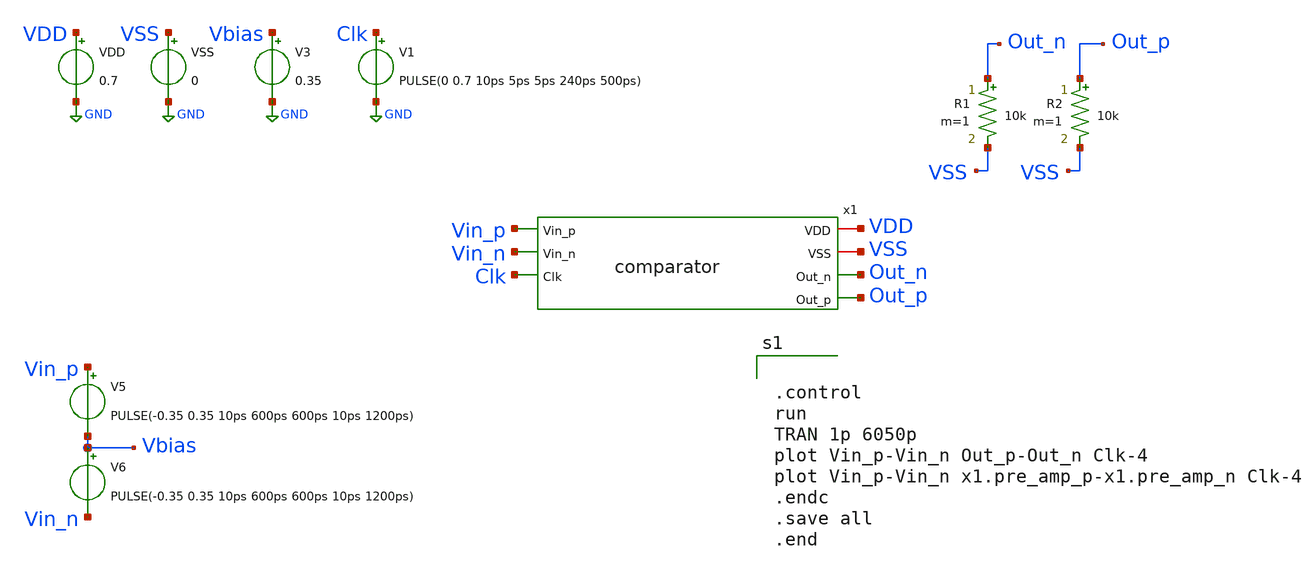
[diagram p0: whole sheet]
** sch_path: xschem/test/comparator_test_triangular_input.sch
* xschem/lib/asap_7nm_nfet.sym:
* Copyright 2021 Stefan Frederik Schippers
* Licensed under the Apache License, Version 2.0 (the "License");
**.subckt comparator_test_triangular_input
V5 Vin_p Vbias PULSE(-0.35 0.35 10ps 600ps 600ps 10ps 1200ps)
V6 Vbias Vin_n PULSE(-0.35 0.35 10ps 600ps 600ps 10ps 1200ps)
VDD VDD GND 0.7
VSS VSS GND 0
V1 Clk GND PULSE(0 0.7 10ps 5ps 5ps 240ps 500ps)
V3 Vbias GND 0.35
R1 Out_n VSS 10k m=1
R2 Out_p VSS 10k m=1
x1 VDD VSS Vin_p Out_n Vin_n Clk Out_p comparator
**** begin user architecture code


.control
run
TRAN 1p 6050p
plot Vin_p-Vin_n Out_p-Out_n Clk-4
plot Vin_p-Vin_n x1.pre_amp_p-x1.pre_amp_n Clk-4
.endc
.save all
.end


**** end user architecture code
**.ends

* expanding   symbol:  /media/psf/avsdcmp_7nm/xschem/src/comparator.sym # of pins=7
** sym_path: xschem/src/comparator.sym
** sch_path: xschem/src/comparator.sch
.subckt comparator VDD VSS Vin_p Out_n Vin_n Clk Out_p
*.iopin VDD
*.iopin VSS
*.ipin Vin_p
*.opin Out_n
*.ipin Vin_n
*.opin Out_p
*.ipin Clk
Xpfet1 Pre_Amp_n Clk_buf VDD VDD asap_7nm_pfet l=7e-009 nfin=7
Xpfet2 Pre_Amp_p Clk_buf VDD VDD asap_7nm_pfet l=7e-009 nfin=7
Xnfet1 Pre_Amp_n Vin_p net1 VSS asap_7nm_nfet l=7e-009 nfin=14
Xnfet2 Pre_Amp_p Vin_n net1 VSS asap_7nm_nfet l=7e-009 nfin=14
Xnfet3 net1 Clk_buf VSS VSS asap_7nm_nfet l=7e-009 nfin=14
Xpfet3 net2 net4 VDD VDD asap_7nm_pfet l=7e-009 nfin=2
Xpfet4 net3 net5 VDD VDD asap_7nm_pfet l=7e-009 nfin=2
Xpfet5 net5 Pre_Amp_n net2 VDD asap_7nm_pfet l=7e-009 nfin=4
Xpfet6 net4 Pre_Amp_p net3 VDD asap_7nm_pfet l=7e-009 nfin=4
Xnfet4 net5 Clk_n VSS VSS asap_7nm_nfet l=7e-009 nfin=10
Xnfet5 net5 net4 VSS VSS asap_7nm_nfet l=7e-009 nfin=10
Xnfet6 net4 net5 VSS VSS asap_7nm_nfet l=7e-009 nfin=10
Xnfet7 net4 Clk_n VSS VSS asap_7nm_nfet l=7e-009 nfin=10
Xpfet7 Clk_n Clk VDD VDD asap_7nm_pfet l=7e-009 nfin=14
Xnfet8 Clk_n Clk VSS VSS asap_7nm_nfet l=7e-009 nfin=14
x3 Out_p net6 VDD VSS buf8
x1 net6 net5 VSS VDD buf8
x2 Out_n net7 VDD VSS buf8
x10 net7 net4 VSS VDD buf8
x4 Clk_buf Clk VDD VSS buf8
.ends


* expanding   symbol:  buf8.sym # of pins=4
** sym_path: xschem/lib/buf8.sym
** sch_path: xschem/lib/buf8.sch
.subckt buf8 Out In VDD VSS
*.iopin VDD
*.iopin VSS
*.ipin In
*.opin Out
Xpfet1 net1 In VDD VDD asap_7nm_pfet l=7e-009 nfin=8
Xnfet1 net1 In VSS VSS asap_7nm_nfet l=7e-009 nfin=8
Xpfet2 Out net1 VDD VDD asap_7nm_pfet l=7e-009 nfin=8
Xnfet2 Out net1 VSS VSS asap_7nm_nfet l=7e-009 nfin=8
.ends

.GLOBAL GND
**** begin user architecture code

.subckt asap_7nm_nfet S G D B l=@l nfin=@nfin
	nnmos_finfet S G D B BSIMCMG_osdi_N l=@l nfin=@nfin
.ends asap_7nm_nfet

.model BSIMCMG_osdi_N BSIMCMG_va (  TYPE = 1
************************************************************
*                         general                          *
************************************************************ version = 107             bulkmod = 1
*+               igcmod  = 1               igbmod  = 0              gidlmod = 1               iimod   = 0
*+               geomod  = 1               rdsmod  = 0              rgatemod= 0               rgeomod = 0
*+               shmod   = 0               nqsmod  = 0              coremod = 0               cgeomod = 0
*+               capmod  = 0               tnom    = 25             eot     = 1e-009          eotbox  = 1.4e-007
*+        eotacc  = 1e-010          tfin    = 6.5e-009       toxp    = 2.1e-009        nbody   = 1e+022
*+          phig    = 4.2466          epsrox  = 3.9            epsrsub = 11.9            easub   = 4.05
*+            ni0sub  = 1.1e+016        bg0sub  = 1.17           nc0sub  = 2.86e+025       nsd     = 2e+026
*+          ngate   = 0               nseg    = 5              l       = 2.1e-008        xl      = 1e-009
*+          lint    = -2e-009         dlc     = 0              dlbin   = 0               hfin    = 3.2e-008
*+        deltaw  = 0               deltawcv= 0              sdterm  = 0               epsrsp  = 3.9
*+             nfin    = 1 toxg    = 1.80e-009
************************************************************
*                            dc                            *
************************************************************ cit     = 0               cdsc    =
*+ 0.01            cdscd   = 0.01            dvt0    = 0.05           dvt1    = 0.47            phin    =
*+ 0.05            eta0    = 0.07            dsub    = 0.35           k1rsce  = 0               lpe0    = 0
*+               dvtshift= 0               qmfactor= 2.5            etaqm   = 0.54            qm0     = 0.001           pqm
*+     = 0.66            u0      = 0.0303         etamob  = 2               up      = 0               ua
*+      = 0.55            eu      = 1.2            ud      = 0               ucs     = 1
*+               rdswmin = 0               rdsw    = 200            wr      = 1               rswmin  = 0
*+               rdwmin  = 0               rshs    = 0              rshd    = 0               vsat    = 70000
*+           deltavsat= 0.2             ksativ  = 2              mexp    = 4               ptwg    = 30              pclm
*+    = 0.05            pclmg   = 0              pdibl1  = 0               pdibl2  = 0.002           drout
*+   = 1               pvag    = 0              fpitch  = 2.7e-008        rth0    = 0.225           cth0
*+    = 1.243e-006      wth0    = 2.6e-007       lcdscd  = 5e-005          lcdscdr = 5e-005          lrdsw
*+   = 0.2             lvsat   = 0
************************************************************
*                         leakage                          *
************************************************************ aigc    = 0.014           bigc    =
*+ 0.005           cigc    = 0.25            dlcigs  = 1e-009         dlcigd  = 1e-009          aigs    =
*+ 0.0115          aigd    = 0.0115          bigs    = 0.00332        bigd    = 0.00332         cigs    =
*+ 0.35            cigd    = 0.35            poxedge = 1.1            agidl   = 1e-012          agisl   =
*+ 1e-012          bgidl   = 10000000        bgisl   = 10000000       egidl   = 0.35            egisl   =
*+ 0.35
************************************************************
*                            rf                            *
************************************************************
************************************************************
*                         junction                         *
************************************************************
************************************************************
*                       capacitance                        *
************************************************************ cfs     = 0               cfd     = 0
*+               cgso    = 1.6e-010        cgdo    = 1.6e-010       cgsl    = 0               cgdl    = 0
*+               ckappas = 0.6             ckappad = 0.6            cgbo    = 0               cgbl    = 0
************************************************************
*                       temperature                        *
************************************************************ tbgasub = 0.000473        tbgbsub = 636
*+             kt1     = 0               kt1l    = 0              ute     = -0.7            utl     = 0
*+               ua1     = 0.001032        ud1     = 0              ucste   = -0.004775       at      = 0.001
*+           ptwgt   = 0.004           tmexp   = 0              prt     = 0               tgidl   = -0.007
*+          igt     = 2.5
************************************************************
*                          noise                           *
************************************************************
**)
.control
pre_osdi ~/ASAP7_FinFET_Inverter_Characterization/Xschem_ASAP7/bsimcmg_arch64.osdi
.endc



.subckt asap_7nm_pfet S G D B l=@l nfin=@nfin
	npmos_finfet S G D B BSIMCMG_osdi_P l=@l nfin=@nfin
.ends asap_7nm_pfet

.model BSIMCMG_osdi_P BSIMCMG_va (  TYPE = 0

************************************************************
*                         general                          *
************************************************************ version = 107             bulkmod = 1
*+               igcmod  = 1               igbmod  = 0              gidlmod = 1               iimod   = 0
*+               geomod  = 1               rdsmod  = 0              rgatemod= 0               rgeomod = 0
*+               shmod   = 0               nqsmod  = 0              coremod = 0               cgeomod = 0
*+               capmod  = 0               tnom    = 25             eot     = 1e-009          eotbox  = 1.4e-007
*+        eotacc  = 3e-010          tfin    = 6.5e-009       toxp    = 2.1e-009        nbody   = 1e+022
*+          phig    = 4.9278          epsrox  = 3.9            epsrsub = 11.9            easub   = 4.05
*+            ni0sub  = 1.1e+016        bg0sub  = 1.17           nc0sub  = 2.86e+025       nsd     = 2e+026
*+          ngate   = 0               nseg    = 5              l       = 2.1e-008        xl      = 1e-009
*+          lint    = -2.5e-009       dlc     = 0              dlbin   = 0               hfin    = 3.2e-008
*+        deltaw  = 0               deltawcv= 0              sdterm  = 0               epsrsp  = 3.9
*+             nfin    = 1 toxg    = 1.8e-009
************************************************************
*                            dc                            *
************************************************************ cit     = 0               cdsc    =
*+ 0.003469        cdscd   = 0.001486        dvt0    = 0.05           dvt1    = 0.36            phin    = 0.05
*+            eta0    = 0.094           dsub    = 0.24           k1rsce  = 0               lpe0    = 0
*+               dvtshift= 0               qmfactor= 0              etaqm   = 0.54            qm0     = 2.183e-012      pqm
*+     = 0.66            u0      = 0.0237         etamob  = 4               up      = 0               ua
*+      = 1.133           eu      = 0.05           ud      = 0.0105          ucs     = 0.2672
*+          rdswmin = 0               rdsw    = 200            wr      = 1               rswmin  = 0
*+               rdwmin  = 0               rshs    = 0              rshd    = 0               vsat    = 60000
*+           deltavsat= 0.17            ksativ  = 1.592          mexp    = 2.491           ptwg    = 25              pclm
*+    = 0.01            pclmg   = 1              pdibl1  = 800             pdibl2  = 0.005704        drout
*+   = 4.97            pvag    = 200            fpitch  = 2.7e-008        rth0    = 0.15            cth0
*+    = 1.243e-006      wth0    = 2.6e-007       lcdscd  = 0               lcdscdr = 0               lrdsw
*+   = 1.3             lvsat   = 1441
************************************************************
*                         leakage                          *
************************************************************ aigc    = 0.007           bigc    =
*+ 0.0015          cigc    = 1               dlcigs  = 5e-009         dlcigd  = 5e-009          aigs    =
*+ 0.006           aigd    = 0.006           bigs    = 0.001944       bigd    = 0.001944        cigs    = 1
*+               cigd    = 1               poxedge = 1.152          agidl   = 2e-012          agisl   = 2e-012
*+          bgidl   = 1.5e+008        bgisl   = 1.5e+008       egidl   = 1.142           egisl   = 1.142
************************************************************
*                            rf                            *
************************************************************
************************************************************
*                         junction                         *
************************************************************
************************************************************
*                       capacitance                        *
************************************************************ cfs     = 0               cfd     = 0
*+               cgso    = 1.6e-010        cgdo    = 1.6e-010       cgsl    = 0               cgdl    = 0
*+               ckappas = 0.6             ckappad = 0.6            cgbo    = 0               cgbl    = 0
************************************************************
*                       temperature                        *
************************************************************ tbgasub = 0.000473        tbgbsub = 636
*+             kt1     = 0               kt1l    = 0              ute     = -1.2            utl     = 0
*+               ua1     = 0.001032        ud1     = 0              ucste   = -0.004775       at      = 0.001
*+           ptwgt   = 0.004           tmexp   = 0              prt     = 0               tgidl   = -0.007
*+          igt     = 2.5
************************************************************
*                          noise                           *
************************************************************
**)
.control
pre_osdi ~/ASAP7_FinFET_Inverter_Characterization/Xschem_ASAP7/bsimcmg_arch64.osdi
.endc


**** end user architecture code
.end
